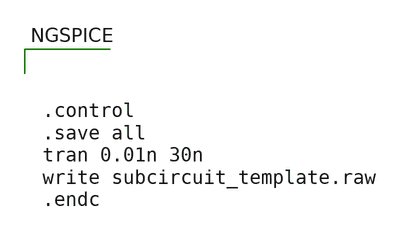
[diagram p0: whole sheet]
** sch_path: images/foss-asic-tools/addons/examples/sky130-analog/util/subcircuit_template.sch
**.subckt subcircuit_template
**** begin user architecture code



.control
.save all
tran 0.01n 30n
write subcircuit_template.raw
.endc



.include $::SKYWATER_MODELS/cells/nfet_01v8/sky130_fd_pr__nfet_01v8__tt.corner.spice
.include $::SKYWATER_MODELS/cells/nfet_01v8_lvt/sky130_fd_pr__nfet_01v8_lvt__tt.corner.spice
.include $::SKYWATER_MODELS/cells/pfet_01v8/sky130_fd_pr__pfet_01v8__tt.corner.spice
.include $::SKYWATER_MODELS/cells/nfet_03v3_nvt/sky130_fd_pr__nfet_03v3_nvt__tt.corner.spice
.include $::SKYWATER_MODELS/cells/nfet_05v0_nvt/sky130_fd_pr__nfet_05v0_nvt__tt.corner.spice
.include $::SKYWATER_MODELS/cells/esd_nfet_01v8/sky130_fd_pr__esd_nfet_01v8__tt.corner.spice
.include $::SKYWATER_MODELS/cells/pfet_01v8_lvt/sky130_fd_pr__pfet_01v8_lvt__tt.corner.spice
.include $::SKYWATER_MODELS/cells/pfet_01v8_hvt/sky130_fd_pr__pfet_01v8_hvt__tt.corner.spice
.include $::SKYWATER_MODELS/cells/esd_pfet_g5v0d10v5/sky130_fd_pr__esd_pfet_g5v0d10v5__tt.corner.spice
.include $::SKYWATER_MODELS/cells/pfet_g5v0d10v5/sky130_fd_pr__pfet_g5v0d10v5__tt.corner.spice
.include $::SKYWATER_MODELS/cells/pfet_g5v0d16v0/sky130_fd_pr__pfet_g5v0d16v0__tt.corner.spice
.include $::SKYWATER_MODELS/cells/nfet_g5v0d10v5/sky130_fd_pr__nfet_g5v0d10v5__tt.corner.spice
.include $::SKYWATER_MODELS/cells/nfet_g5v0d16v0/sky130_fd_pr__nfet_g5v0d16v0__tt_discrete.corner.spice
.include $::SKYWATER_MODELS/cells/esd_nfet_g5v0d10v5/sky130_fd_pr__esd_nfet_g5v0d10v5__tt.corner.spice
.include $::SKYWATER_MODELS/models/corners/tt/nonfet.spice
* Mismatch parameters
.include $::SKYWATER_MODELS/cells/nfet_01v8/sky130_fd_pr__nfet_01v8__mismatch.corner.spice
.include $::SKYWATER_MODELS/cells/pfet_01v8/sky130_fd_pr__pfet_01v8__mismatch.corner.spice
.include $::SKYWATER_MODELS/cells/nfet_01v8_lvt/sky130_fd_pr__nfet_01v8_lvt__mismatch.corner.spice
.include $::SKYWATER_MODELS/cells/pfet_01v8_lvt/sky130_fd_pr__pfet_01v8_lvt__mismatch.corner.spice
.include $::SKYWATER_MODELS/cells/pfet_01v8_hvt/sky130_fd_pr__pfet_01v8_hvt__mismatch.corner.spice
.include $::SKYWATER_MODELS/cells/nfet_g5v0d10v5/sky130_fd_pr__nfet_g5v0d10v5__mismatch.corner.spice
.include $::SKYWATER_MODELS/cells/pfet_g5v0d10v5/sky130_fd_pr__pfet_g5v0d10v5__mismatch.corner.spice
.include $::SKYWATER_MODELS/cells/nfet_05v0_nvt/sky130_fd_pr__nfet_05v0_nvt__mismatch.corner.spice
.include $::SKYWATER_MODELS/cells/nfet_03v3_nvt/sky130_fd_pr__nfet_03v3_nvt__mismatch.corner.spice
* Resistor$::SKYWATER_MODELS/Capacitor
.include $::SKYWATER_MODELS/models/r+c/res_typical__cap_typical.spice
.include $::SKYWATER_MODELS/models/r+c/res_typical__cap_typical__lin.spice
* Special cells
.include $::SKYWATER_MODELS/models/corners/tt/specialized_cells.spice
* All models
.include $::SKYWATER_MODELS/models/all.spice
* Corner
.include $::SKYWATER_MODELS/models/corners/tt/rf.spice

**** end user architecture code
**.ends
**** begin user architecture code
[sky130_models]
**** end user architecture code
.end
